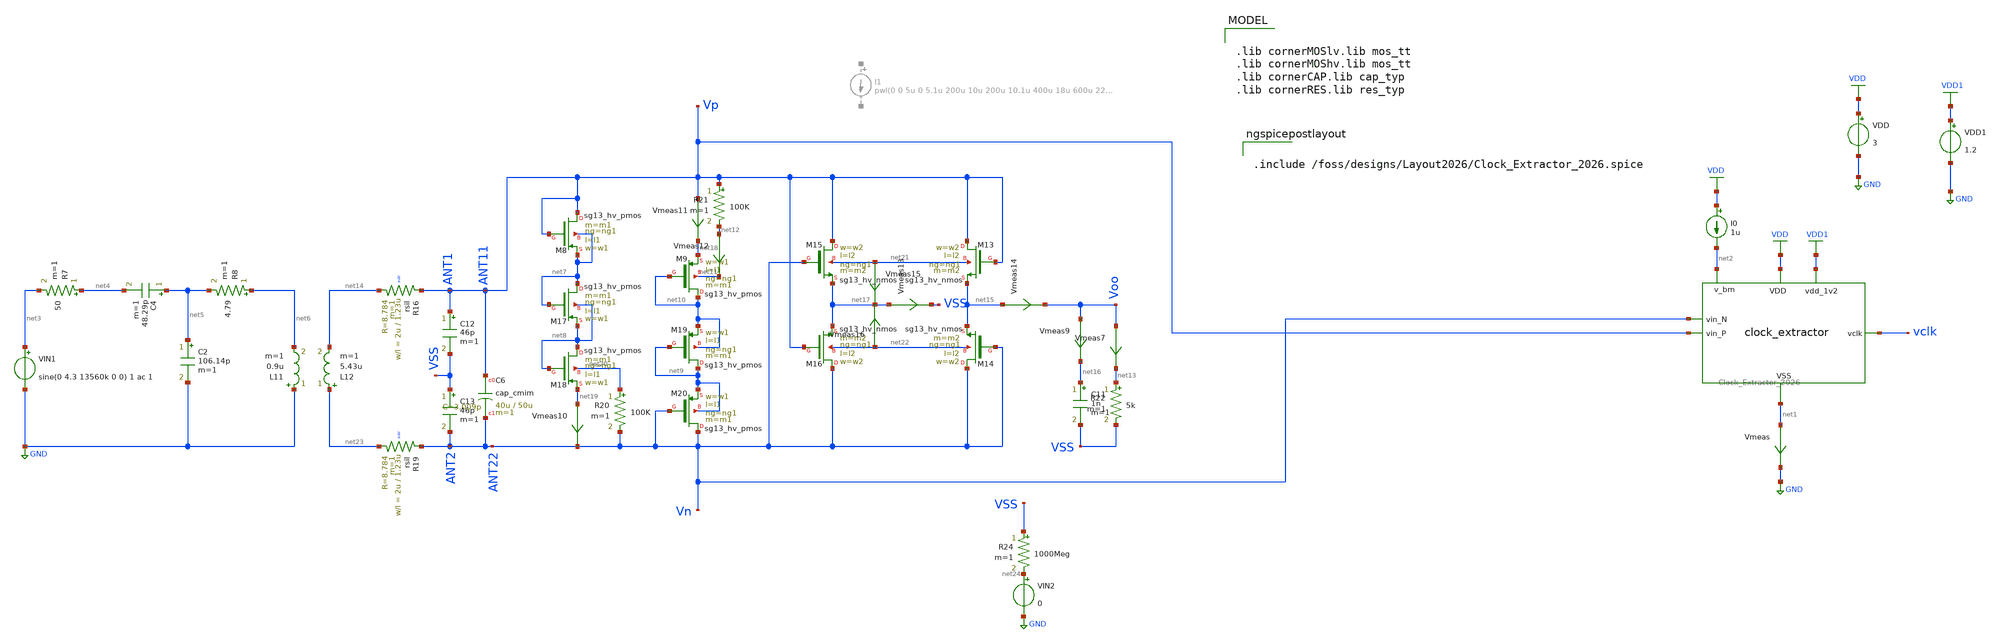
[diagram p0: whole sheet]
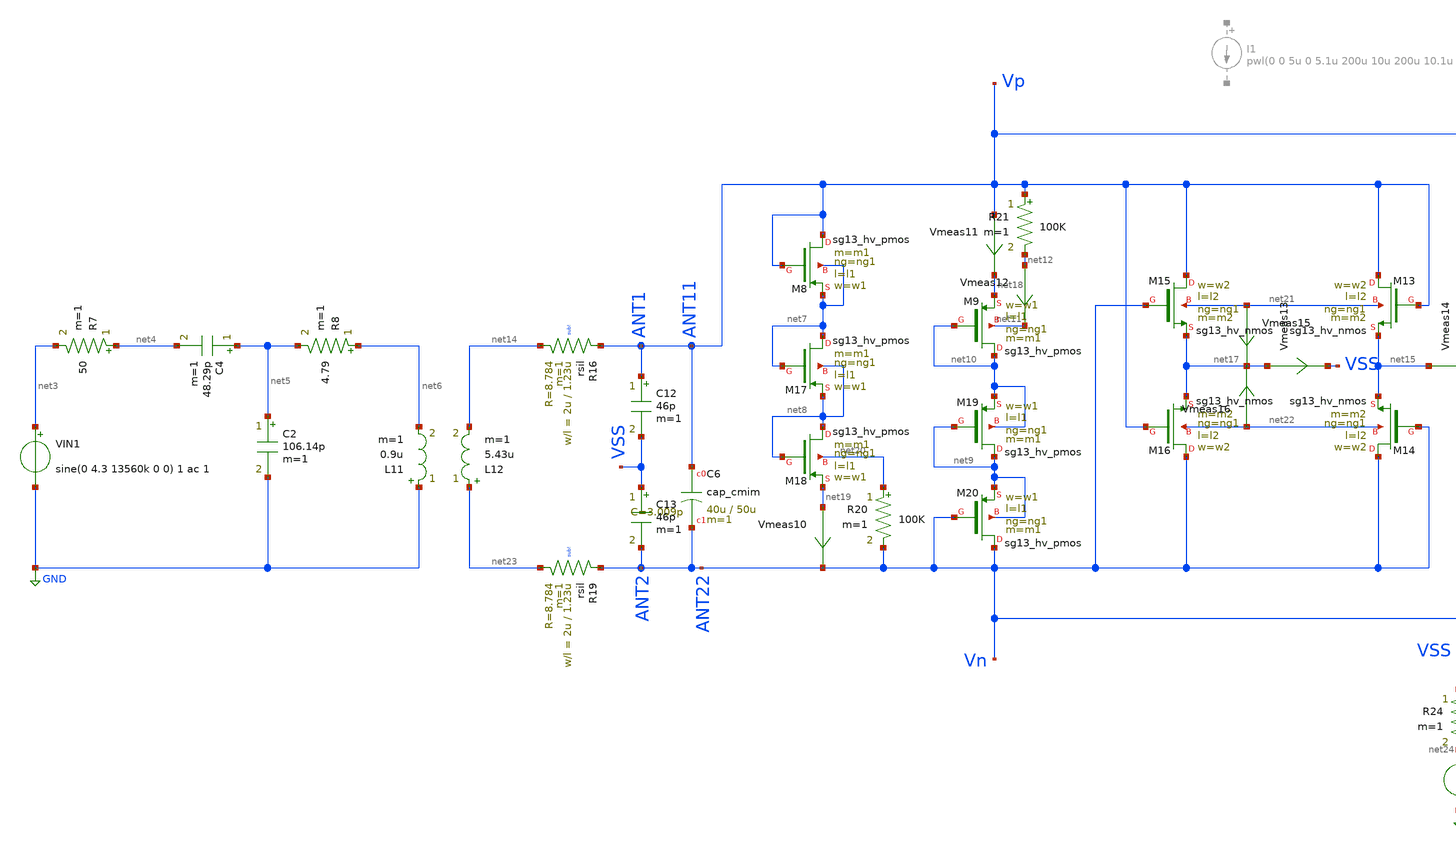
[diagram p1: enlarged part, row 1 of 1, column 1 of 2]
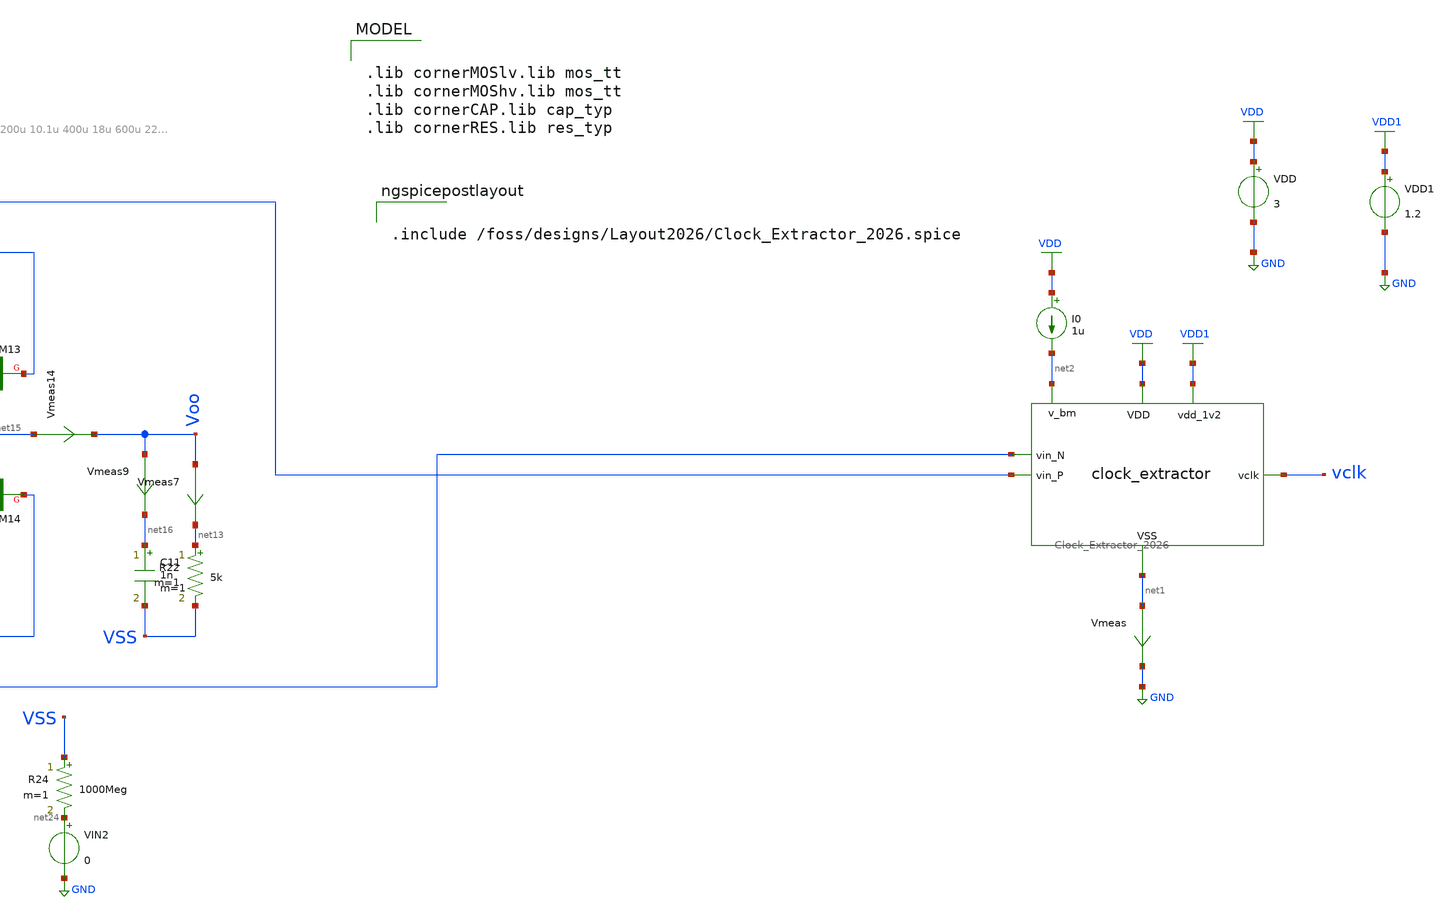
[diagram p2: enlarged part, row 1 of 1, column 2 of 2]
** sch_path: dependencies/ClockExtractor/ClockExtractor-main/schematic/xschem/schematic/postlayout_TRAN_clock_extractor_2026.sch
**.subckt postlayout_TRAN_clock_extractor_2026
X1 VDD net1 VDD1 ANT22 ANT11 net2 vclk Clock_Extractor_2026
I0 VDD net2 1u
VDD VDD GND 3
VDD1 VDD1 GND 1.2
VIN1 net3 GND sine(0 4.3 13560k 0 0) 1 ac 1

L11 GND net6 0.9u m=1
C2 net5 GND 106.14p m=1
R7 net4 net3 50 m=1
C4 net5 net4 48.29p m=1
R8 net6 net5 4.79 m=1
L12 net23 net14 5.43u m=1
XR16 ANT11 net14 sub! rsil w=2u l=1.23u m=1 mm_ok=1
XR19 ANT22 net23 sub! rsil w=2u l=1.23u m=1 mm_ok=1
XC6 ANT11 ANT22 cap_cmim w=40u l=50u m=1 mm_ok=1
XM8 ANT11 ANT11 net7 net7 sg13_hv_pmos w=w1 l=l1 ng=ng1 m=m1 mm_ok=1
XM9 net10 net10 net18 net11 sg13_hv_pmos w=w1 l=l1 ng=ng1 m=m1 mm_ok=1
R20 net20 ANT22 100K m=1
R21 ANT11 net12 100K m=1
XM13 ANT11 ANT11 net15 net21 sg13_hv_nmos w=w2 l=l2 ng=ng1 m=m2 mm_ok=1
XM14 ANT22 ANT22 net15 net22 sg13_hv_nmos w=w2 l=l2 ng=ng1 m=m2 mm_ok=1
C11 net16 VSS 1n m=1
R22 net13 VSS 5k m=1
Vmeas12 net12 net11 0
.save i(vmeas12)
C12 ANT11 VSS 46p m=1
C13 VSS ANT22 46p m=1
XM15 ANT11 ANT22 net17 net21 sg13_hv_nmos w=w2 l=l2 ng=ng1 m=m2 mm_ok=1
XM16 ANT22 ANT11 net17 net22 sg13_hv_nmos w=w2 l=l2 ng=ng1 m=m2 mm_ok=1
XM17 net7 net7 net8 net8 sg13_hv_pmos w=w1 l=l1 ng=ng1 m=m1 mm_ok=1
XM18 net8 net8 net19 net20 sg13_hv_pmos w=w1 l=l1 ng=ng1 m=m1 mm_ok=1
XM19 net9 net9 net10 net10 sg13_hv_pmos w=w1 l=l1 ng=ng1 m=m1 mm_ok=1
XM20 ANT22 ANT22 net9 net9 sg13_hv_pmos w=w1 l=l1 ng=ng1 m=m1 mm_ok=1
Vmeas7 Voo net13 0
.save i(vmeas7)
Vmeas9 Voo net16 0
.save i(vmeas9)
Vmeas10 net19 ANT22 0
.save i(vmeas10)
Vmeas11 ANT11 net18 0
.save i(vmeas11)
Vmeas13 net17 VSS 0
.save i(vmeas13)
Vmeas14 net15 Voo 0
.save i(vmeas14)
Vmeas15 net21 net17 0
.save i(vmeas15)
Vmeas16 net22 net17 0
.save i(vmeas16)
R24 VSS net24 1000Meg m=1
VIN2 net24 GND 0
Vmeas net1 GND 0
.save i(vmeas)
**** begin user architecture code

.lib cornerMOSlv.lib mos_tt
.lib cornerMOShv.lib mos_tt
.lib cornerCAP.lib cap_typ
.lib cornerRES.lib res_typ



.param temp=27
.options rshunt =1e12
.param w1=5u
.param w2=10u
.param l1=0.5u
.param l2=1u
.param ng1=1
.param m1=20
.param m2=10
.param Coef=0.1
.save all
.control

* Transient simulation
tran 50p 3.5u
plot vclk
plot i(Vmeas7)
plot i(Vmeas)

meas tran avg_current AVG I(VDD)  from=1u to=1.5u
let  power_VDD=3*avg_current
meas tran avg_current_1 AVG I(VDD1) from=1u to=1.5u
let  power_VDD1=1.2*avg_current_1
let total_power=power_VDD + power_VDD1

meas tran thigh TRIG v(vclk) VAL=1.08 RISE=39 TARG v(vclk) VAL=1.08 FALL=39
meas tran tlow TRIG  v(vclk)  VAL=0.12 FALL=39  TARG v(vclk) VAL=0.12 RISE=40

//meas tran thigh TRIG v(vclk) VAl=0.6 RISE=25 TARG v(vclk) VAl=0.6 FALL=25
//meas tran tlow  TRIG v(vclk) VAl=0.6 FALL=25 TARG v(vclk) VAl=0.6 RISE=26
  * rise time and fall time
meas tran t100 when v(vclk)=0.12 rise=25
meas tran t90  when  v(vclk)=1.08 rise=25

let RiseTime = t90 - t100

meas tran t90_f when v(vclk)=1.08 fall=25
meas tran t10_f when v(vclk)=0.12 fall=25

let FallTime = t10_f - t90_f



meas tran t19 when v(vclk)=0.6 rise=43
meas tran t20 when v(vclk)=0.6 rise=44
let period1 =(t20 - t19)
let freq1 =1/period1

meas tran t21 when v(vclk)=0.6 rise=45
let period2 =(t21 - t20)
let freq2 =1/period2


let duty_cycle =thigh/(period1)*100

print freq1
print freq2

print thigh
print tlow
print RiseTime
print FallTime
print duty_cycle
print total_power


 write postlayout_TRAN_clock_extractor_2026.raw
.endc
K1 L11 L12  0.7



.include /foss/designs/Layout2026/Clock_Extractor_2026.spice

**** end user architecture code
**.ends
.GLOBAL VDD
.GLOBAL VDD1
.GLOBAL GND
.end
